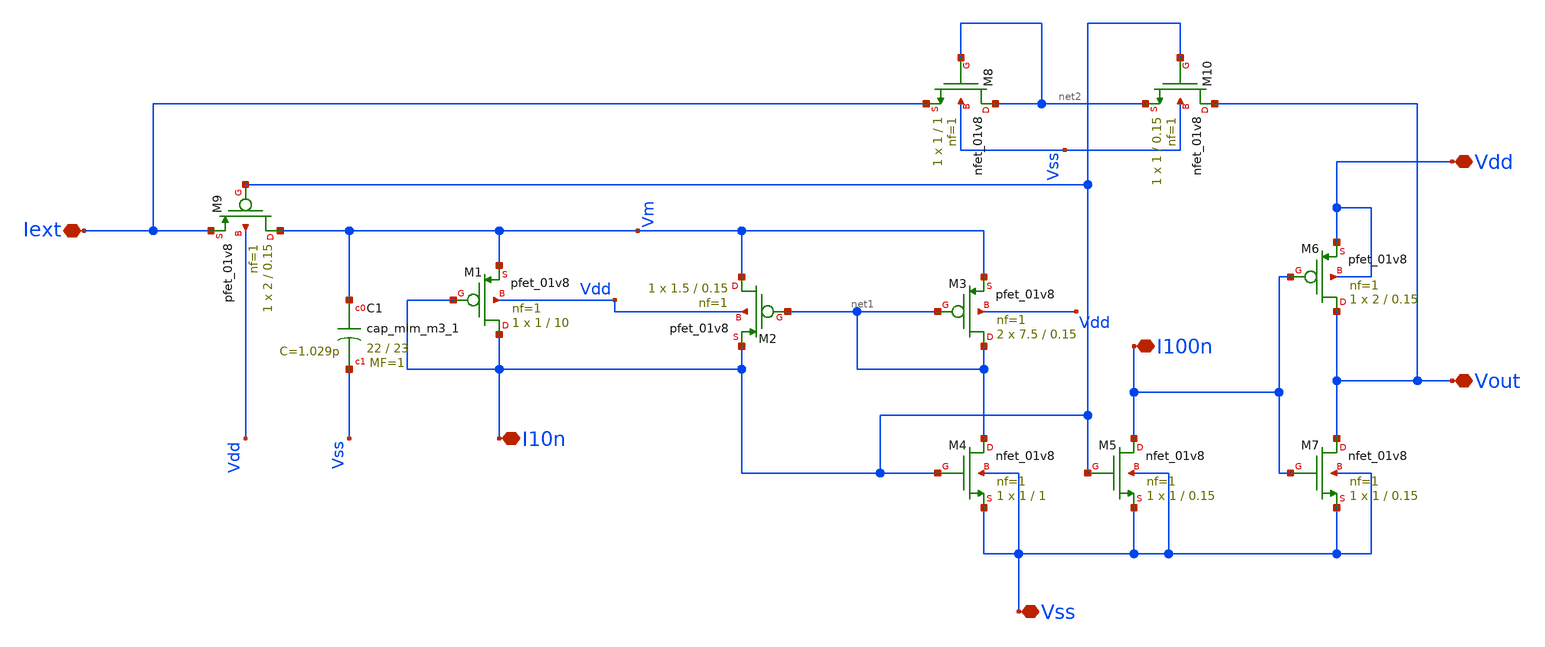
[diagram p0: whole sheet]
** sch_path: MANCILLA/NeuronaFinal.sch
**.subckt NeuronaFinal Vout I100n Vdd Vss Iext I10n
*.iopin Vout
*.iopin I100n
*.iopin Vdd
*.iopin Vss
*.iopin Iext
*.iopin I10n
XM1 I10n I10n Vm Vdd sky130_fd_pr__pfet_01v8 L=10 W=1 nf=1 ad='int((nf+1)/2) * W/nf * 0.29' as='int((nf+2)/2) * W/nf * 0.29'
+ pd='2*int((nf+1)/2) * (W/nf + 0.29)' ps='2*int((nf+2)/2) * (W/nf + 0.29)' nrd='0.29 / W' nrs='0.29 / W'
+ sa=0 sb=0 sd=0 mult=1 m=1
XM2 Vm net1 I10n Vdd sky130_fd_pr__pfet_01v8 L=0.15 W=1.5 nf=1 ad='int((nf+1)/2) * W/nf * 0.29' as='int((nf+2)/2) * W/nf * 0.29'
+ pd='2*int((nf+1)/2) * (W/nf + 0.29)' ps='2*int((nf+2)/2) * (W/nf + 0.29)' nrd='0.29 / W' nrs='0.29 / W'
+ sa=0 sb=0 sd=0 mult=1 m=1
XM3 net1 net1 Vm Vdd sky130_fd_pr__pfet_01v8 L=0.15 W=7.5 nf=1 ad='int((nf+1)/2) * W/nf * 0.29' as='int((nf+2)/2) * W/nf * 0.29'
+ pd='2*int((nf+1)/2) * (W/nf + 0.29)' ps='2*int((nf+2)/2) * (W/nf + 0.29)' nrd='0.29 / W' nrs='0.29 / W'
+ sa=0 sb=0 sd=0 mult=2 m=2
XM4 net1 I10n Vss Vss sky130_fd_pr__nfet_01v8 L=1 W=1 nf=1 ad='int((nf+1)/2) * W/nf * 0.29' as='int((nf+2)/2) * W/nf * 0.29'
+ pd='2*int((nf+1)/2) * (W/nf + 0.29)' ps='2*int((nf+2)/2) * (W/nf + 0.29)' nrd='0.29 / W' nrs='0.29 / W'
+ sa=0 sb=0 sd=0 mult=1 m=1
XM5 I100n I10n Vss Vss sky130_fd_pr__nfet_01v8 L=0.15 W=1 nf=1 ad='int((nf+1)/2) * W/nf * 0.29' as='int((nf+2)/2) * W/nf * 0.29'
+ pd='2*int((nf+1)/2) * (W/nf + 0.29)' ps='2*int((nf+2)/2) * (W/nf + 0.29)' nrd='0.29 / W' nrs='0.29 / W'
+ sa=0 sb=0 sd=0 mult=1 m=1
XM6 Vout I100n Vdd Vdd sky130_fd_pr__pfet_01v8 L=0.15 W=2 nf=1 ad='int((nf+1)/2) * W/nf * 0.29' as='int((nf+2)/2) * W/nf * 0.29'
+ pd='2*int((nf+1)/2) * (W/nf + 0.29)' ps='2*int((nf+2)/2) * (W/nf + 0.29)' nrd='0.29 / W' nrs='0.29 / W'
+ sa=0 sb=0 sd=0 mult=1 m=1
XM7 Vout I100n Vss Vss sky130_fd_pr__nfet_01v8 L=0.15 W=1 nf=1 ad='int((nf+1)/2) * W/nf * 0.29' as='int((nf+2)/2) * W/nf * 0.29'
+ pd='2*int((nf+1)/2) * (W/nf + 0.29)' ps='2*int((nf+2)/2) * (W/nf + 0.29)' nrd='0.29 / W' nrs='0.29 / W'
+ sa=0 sb=0 sd=0 mult=1 m=1
XM8 net2 net2 Iext Vss sky130_fd_pr__nfet_01v8 L=1 W=1 nf=1 ad='int((nf+1)/2) * W/nf * 0.29' as='int((nf+2)/2) * W/nf * 0.29'
+ pd='2*int((nf+1)/2) * (W/nf + 0.29)' ps='2*int((nf+2)/2) * (W/nf + 0.29)' nrd='0.29 / W' nrs='0.29 / W'
+ sa=0 sb=0 sd=0 mult=1 m=1
XM9 Vm I10n Iext Vdd sky130_fd_pr__pfet_01v8 L=0.15 W=2 nf=1 ad='int((nf+1)/2) * W/nf * 0.29' as='int((nf+2)/2) * W/nf * 0.29'
+ pd='2*int((nf+1)/2) * (W/nf + 0.29)' ps='2*int((nf+2)/2) * (W/nf + 0.29)' nrd='0.29 / W' nrs='0.29 / W'
+ sa=0 sb=0 sd=0 mult=1 m=1
XM10 Vout I10n net2 Vss sky130_fd_pr__nfet_01v8 L=0.15 W=1 nf=1 ad='int((nf+1)/2) * W/nf * 0.29' as='int((nf+2)/2) * W/nf * 0.29'
+ pd='2*int((nf+1)/2) * (W/nf + 0.29)' ps='2*int((nf+2)/2) * (W/nf + 0.29)' nrd='0.29 / W' nrs='0.29 / W'
+ sa=0 sb=0 sd=0 mult=1 m=1
XC1 Vm Vss sky130_fd_pr__cap_mim_m3_1 W=22 L=23 MF=1 m=1
**.ends
.end
